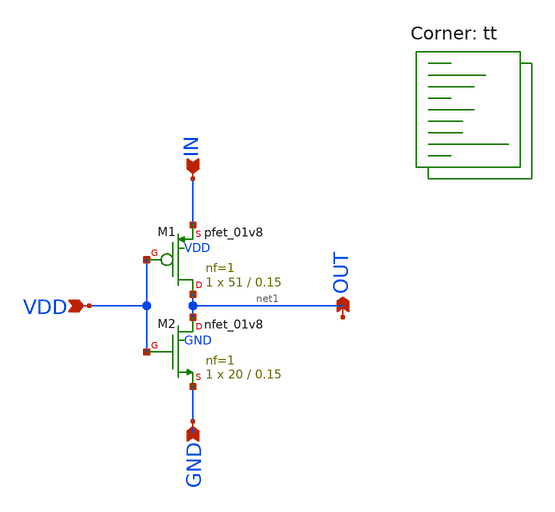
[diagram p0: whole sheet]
** sch_path: inverter.sch
**.subckt inverter VDD IN OUT GND
*.ipin VDD
*.ipin IN
*.opin OUT
*.ipin GND
XM2 net1 VDD GND GND sky130_fd_pr__nfet_01v8 L=0.15 W=20 nf=1 ad='int((nf+1)/2) * W/nf * 0.29' as='int((nf+2)/2) * W/nf * 0.29'
+ pd='2*int((nf+1)/2) * (W/nf + 0.29)' ps='2*int((nf+2)/2) * (W/nf + 0.29)' nrd='0.29 / W' nrs='0.29 / W'
+ sa=0 sb=0 sd=0 mult=1 m=1
XM1 net1 VDD IN VDD sky130_fd_pr__pfet_01v8 L=0.15 W=51 nf=1 ad='int((nf+1)/2) * W/nf * 0.29' as='int((nf+2)/2) * W/nf * 0.29'
+ pd='2*int((nf+1)/2) * (W/nf + 0.29)' ps='2*int((nf+2)/2) * (W/nf + 0.29)' nrd='0.29 / W' nrs='0.29 / W'
+ sa=0 sb=0 sd=0 mult=1 m=1
**** begin user architecture code



.options savecurrents

.control
save all
*dc vgs 0 1.8 0.01 vdd 0.01 1.8 0.2
*dc vdd 0.01 1.8 0.01
dc vgs 0 1.8 0.01
let id_nmos=@m.xm3.msky130_fd_pr__nfet_01v8[id]
let id_pmos=@m.xm4.msky130_fd_pr__pfet_01v8[id]

plot deriv(sqrt(id_nmos))^2/deriv(sqrt(id_pmos))^2 title 'V_DD characteristic' xlabel 'V_DD' ylabel 'Ratio of derivatives'

write characterization.raw

set appendwrite
.endc


.lib $::SKYWATER_MODELS/sky130.lib.spice tt
**** end user architecture code
**.ends
.end
